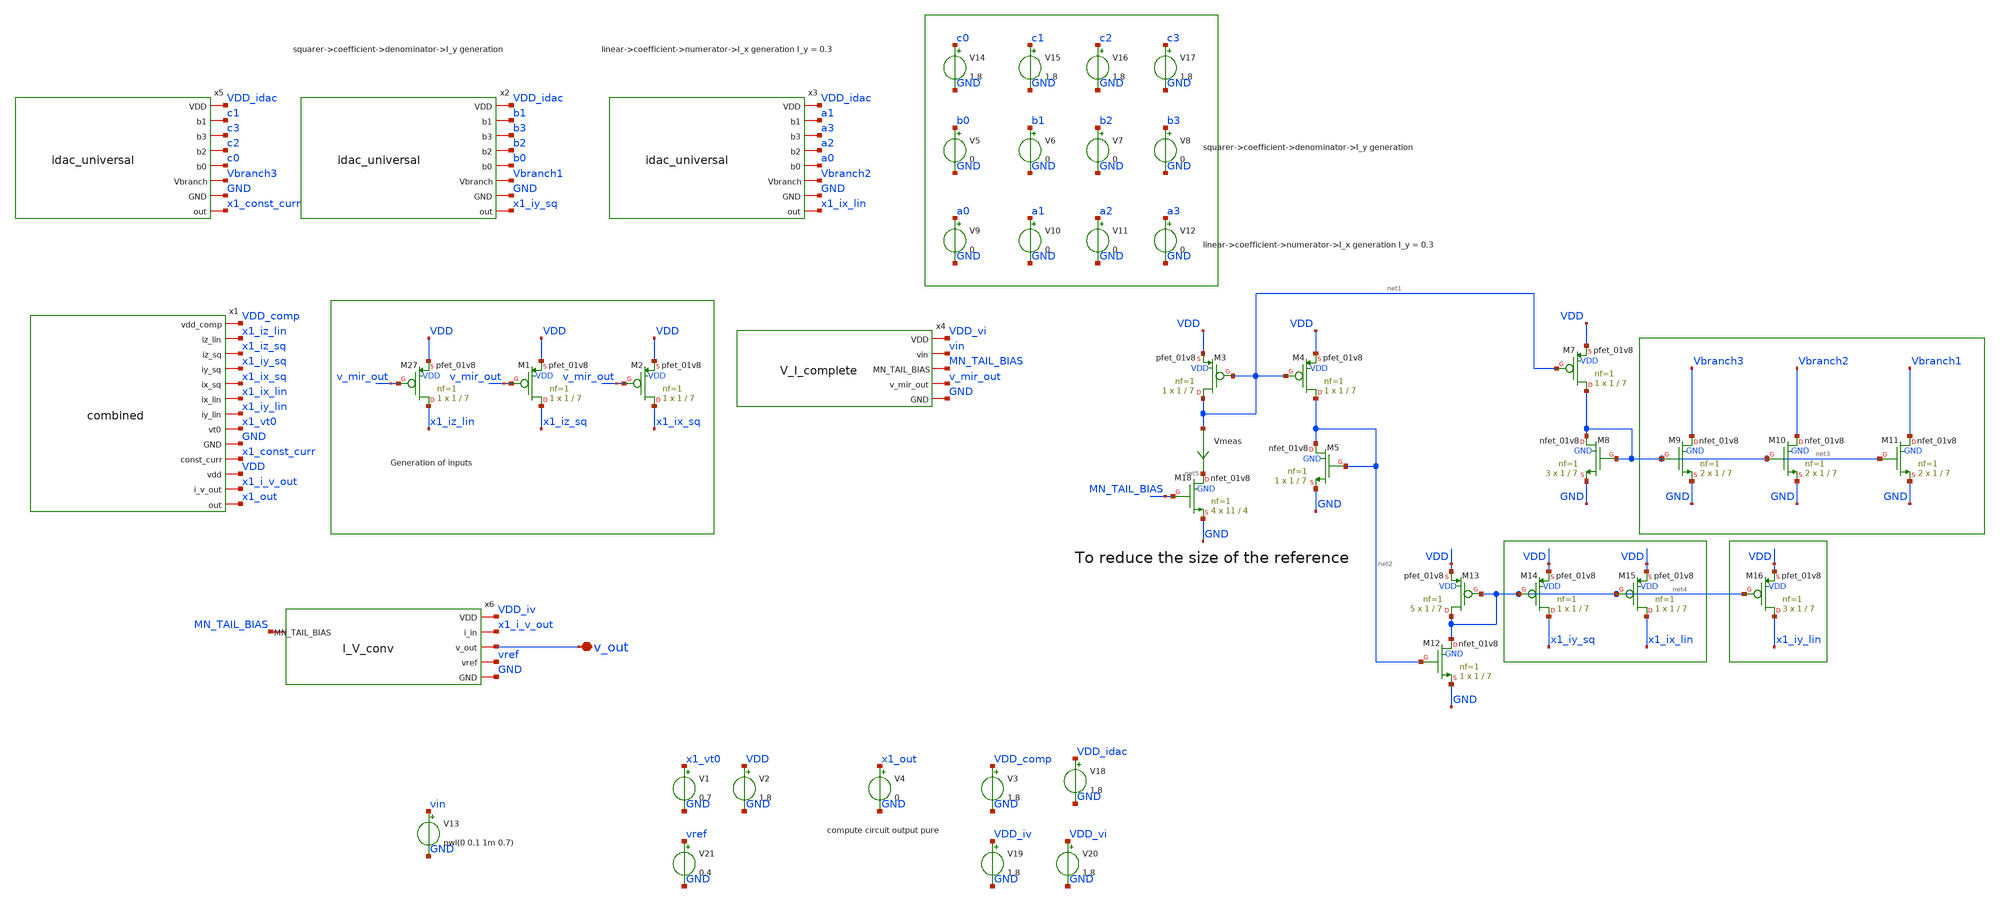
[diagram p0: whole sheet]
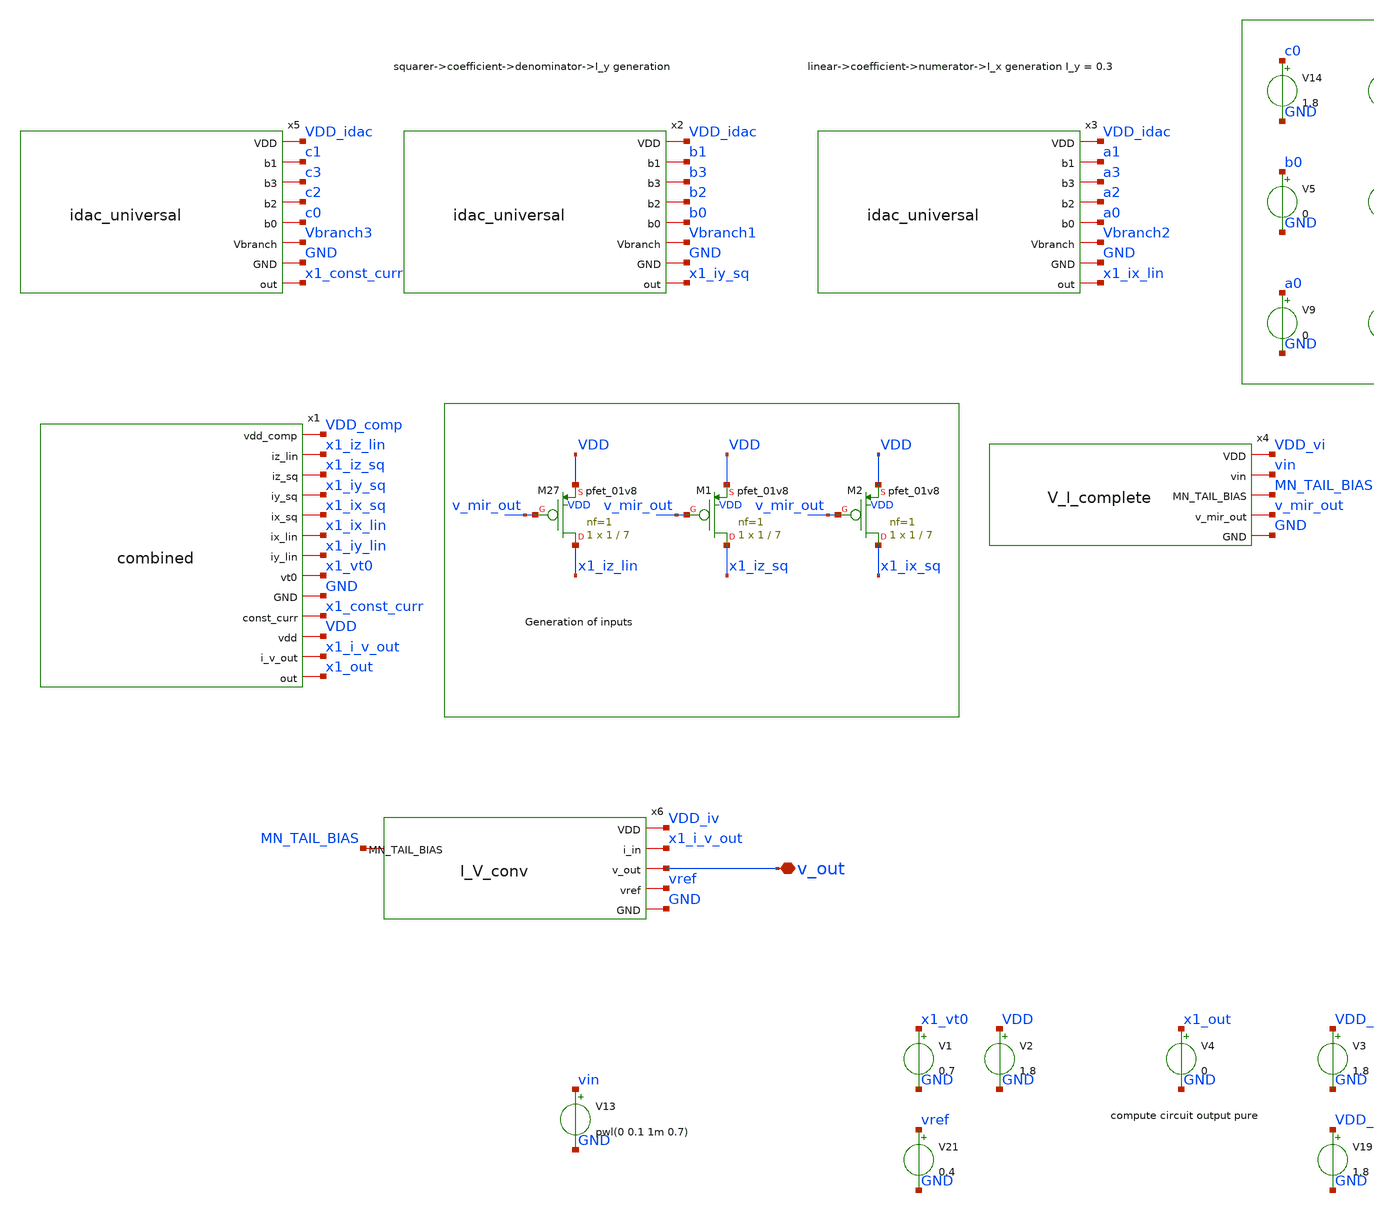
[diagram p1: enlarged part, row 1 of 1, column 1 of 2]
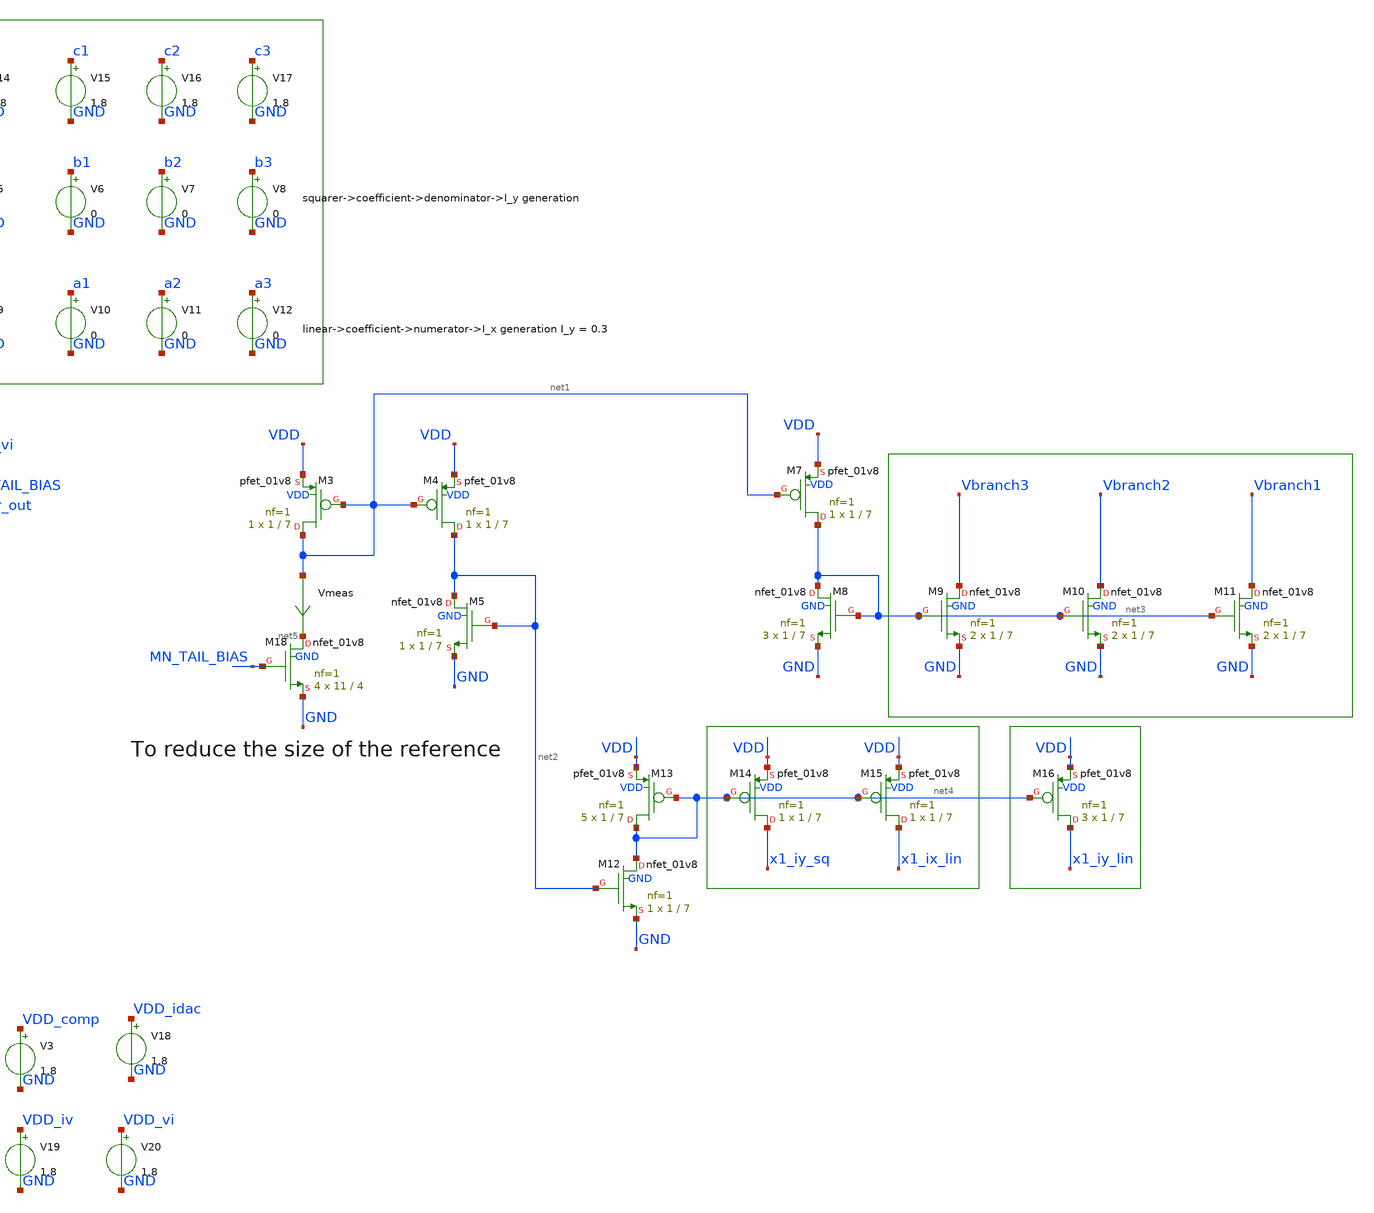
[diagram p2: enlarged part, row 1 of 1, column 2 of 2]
** sch_path: xschem/top/compute_system.sch
**.subckt compute_system v_out
*.iopin v_out
V5 b0 GND 0
V6 b1 GND 0
V7 b2 GND 0
V8 b3 GND 0
V9 a0 GND 0
V10 a1 GND 0
V11 a2 GND 0
V12 a3 GND 0
V1 x1_vt0 GND 0.7
V2 VDD GND 1.8
V4 x1_out GND 0
XM27 x1_iz_lin v_mir_out VDD VDD sky130_fd_pr__pfet_01v8 L=7 W=1 nf=1 ad='int((1 + 1)/2) * 1 / 1 * 0.29'
+ as='int((1 + 2)/2) * 1 / 1 * 0.29' pd='2*int((1 + 1)/2) * (1 / 1 + 0.29)' ps='2*int((1 + 2)/2) * (1 / 1 + 0.29)'
+ nrd='0.29 / 1 ' nrs='0.29 / 1 ' sa=0 sb=0 sd=0 mult=1 m=1
XM1 x1_iz_sq v_mir_out VDD VDD sky130_fd_pr__pfet_01v8 L=7 W=1 nf=1 ad='int((1 + 1)/2) * 1 / 1 * 0.29'
+ as='int((1 + 2)/2) * 1 / 1 * 0.29' pd='2*int((1 + 1)/2) * (1 / 1 + 0.29)' ps='2*int((1 + 2)/2) * (1 / 1 + 0.29)'
+ nrd='0.29 / 1 ' nrs='0.29 / 1 ' sa=0 sb=0 sd=0 mult=1 m=1
XM2 x1_ix_sq v_mir_out VDD VDD sky130_fd_pr__pfet_01v8 L=7 W=1 nf=1 ad='int((1 + 1)/2) * 1 / 1 * 0.29'
+ as='int((1 + 2)/2) * 1 / 1 * 0.29' pd='2*int((1 + 1)/2) * (1 / 1 + 0.29)' ps='2*int((1 + 2)/2) * (1 / 1 + 0.29)'
+ nrd='0.29 / 1 ' nrs='0.29 / 1 ' sa=0 sb=0 sd=0 mult=1 m=1
V14 c0 GND 1.8
V15 c1 GND 1.8
V16 c2 GND 1.8
V17 c3 GND 1.8
XM18 net5 MN_TAIL_BIAS GND GND sky130_fd_pr__nfet_01v8 L=4 W=11 nf=1 ad='int((nf+1)/2) * W/nf * 0.29'
+ as='int((nf+2)/2) * W/nf * 0.29' pd='2*int((nf+1)/2) * (W/nf + 0.29)' ps='2*int((nf+2)/2) * (W/nf + 0.29)'
+ nrd='0.29 / W' nrs='0.29 / W' sa=0 sb=0 sd=0 mult=4 m=4
XM3 net1 net1 VDD VDD sky130_fd_pr__pfet_01v8 L=7 W=1 nf=1 ad='int((1 + 1)/2) * 1 / 1 * 0.29' as='int((1 + 2)/2) * 1 / 1 * 0.29'
+ pd='2*int((1 + 1)/2) * (1 / 1 + 0.29)' ps='2*int((1 + 2)/2) * (1 / 1 + 0.29)' nrd='0.29 / 1 ' nrs='0.29 / 1 '
+ sa=0 sb=0 sd=0 mult=1 m=1
XM4 net2 net1 VDD VDD sky130_fd_pr__pfet_01v8 L=7 W=1 nf=1 ad='int((1 + 1)/2) * 1 / 1 * 0.29' as='int((1 + 2)/2) * 1 / 1 * 0.29'
+ pd='2*int((1 + 1)/2) * (1 / 1 + 0.29)' ps='2*int((1 + 2)/2) * (1 / 1 + 0.29)' nrd='0.29 / 1 ' nrs='0.29 / 1 '
+ sa=0 sb=0 sd=0 mult=1 m=1
XM5 net2 net2 GND GND sky130_fd_pr__nfet_01v8 L=7 W=1 nf=1 ad='int((nf+1)/2) * W/nf * 0.29' as='int((nf+2)/2) * W/nf * 0.29'
+ pd='2*int((nf+1)/2) * (W/nf + 0.29)' ps='2*int((nf+2)/2) * (W/nf + 0.29)' nrd='0.29 / W' nrs='0.29 / W'
+ sa=0 sb=0 sd=0 mult=1 m=1
Vmeas net1 net5 0
.save i(vmeas)
XM7 net3 net1 VDD VDD sky130_fd_pr__pfet_01v8 L=7 W=1 nf=1 ad='int((1 + 1)/2) * 1 / 1 * 0.29' as='int((1 + 2)/2) * 1 / 1 * 0.29'
+ pd='2*int((1 + 1)/2) * (1 / 1 + 0.29)' ps='2*int((1 + 2)/2) * (1 / 1 + 0.29)' nrd='0.29 / 1 ' nrs='0.29 / 1 '
+ sa=0 sb=0 sd=0 mult=1 m=1
XM8 net3 net3 GND GND sky130_fd_pr__nfet_01v8 L=7 W=1 nf=1 ad='int((nf+1)/2) * W/nf * 0.29' as='int((nf+2)/2) * W/nf * 0.29'
+ pd='2*int((nf+1)/2) * (W/nf + 0.29)' ps='2*int((nf+2)/2) * (W/nf + 0.29)' nrd='0.29 / W' nrs='0.29 / W'
+ sa=0 sb=0 sd=0 mult=3 m=3
XM9 Vbranch3 net3 GND GND sky130_fd_pr__nfet_01v8 L=7 W=1 nf=1 ad='int((nf+1)/2) * W/nf * 0.29' as='int((nf+2)/2) * W/nf * 0.29'
+ pd='2*int((nf+1)/2) * (W/nf + 0.29)' ps='2*int((nf+2)/2) * (W/nf + 0.29)' nrd='0.29 / W' nrs='0.29 / W'
+ sa=0 sb=0 sd=0 mult=2 m=2
XM10 Vbranch2 net3 GND GND sky130_fd_pr__nfet_01v8 L=7 W=1 nf=1 ad='int((nf+1)/2) * W/nf * 0.29' as='int((nf+2)/2) * W/nf * 0.29'
+ pd='2*int((nf+1)/2) * (W/nf + 0.29)' ps='2*int((nf+2)/2) * (W/nf + 0.29)' nrd='0.29 / W' nrs='0.29 / W'
+ sa=0 sb=0 sd=0 mult=2 m=2
XM11 Vbranch1 net3 GND GND sky130_fd_pr__nfet_01v8 L=7 W=1 nf=1 ad='int((nf+1)/2) * W/nf * 0.29' as='int((nf+2)/2) * W/nf * 0.29'
+ pd='2*int((nf+1)/2) * (W/nf + 0.29)' ps='2*int((nf+2)/2) * (W/nf + 0.29)' nrd='0.29 / W' nrs='0.29 / W'
+ sa=0 sb=0 sd=0 mult=2 m=2
XM12 net4 net2 GND GND sky130_fd_pr__nfet_01v8 L=7 W=1 nf=1 ad='int((nf+1)/2) * W/nf * 0.29' as='int((nf+2)/2) * W/nf * 0.29'
+ pd='2*int((nf+1)/2) * (W/nf + 0.29)' ps='2*int((nf+2)/2) * (W/nf + 0.29)' nrd='0.29 / W' nrs='0.29 / W'
+ sa=0 sb=0 sd=0 mult=1 m=1
XM13 net4 net4 VDD VDD sky130_fd_pr__pfet_01v8 L=7 W=1 nf=1 ad='int((1 + 1)/2) * 1 / 1 * 0.29' as='int((1 + 2)/2) * 1 / 1 * 0.29'
+ pd='2*int((1 + 1)/2) * (1 / 1 + 0.29)' ps='2*int((1 + 2)/2) * (1 / 1 + 0.29)' nrd='0.29 / 1 ' nrs='0.29 / 1 '
+ sa=0 sb=0 sd=0 mult=5 m=5
XM14 x1_iy_sq net4 VDD VDD sky130_fd_pr__pfet_01v8 L=7 W=1 nf=1 ad='int((1 + 1)/2) * 1 / 1 * 0.29' as='int((1 + 2)/2) * 1 / 1 * 0.29'
+ pd='2*int((1 + 1)/2) * (1 / 1 + 0.29)' ps='2*int((1 + 2)/2) * (1 / 1 + 0.29)' nrd='0.29 / 1 ' nrs='0.29 / 1 '
+ sa=0 sb=0 sd=0 mult=1 m=1
XM15 x1_ix_lin net4 VDD VDD sky130_fd_pr__pfet_01v8 L=7 W=1 nf=1 ad='int((1 + 1)/2) * 1 / 1 * 0.29' as='int((1 + 2)/2) * 1 / 1 * 0.29'
+ pd='2*int((1 + 1)/2) * (1 / 1 + 0.29)' ps='2*int((1 + 2)/2) * (1 / 1 + 0.29)' nrd='0.29 / 1 ' nrs='0.29 / 1 '
+ sa=0 sb=0 sd=0 mult=1 m=1
XM16 x1_iy_lin net4 VDD VDD sky130_fd_pr__pfet_01v8 L=7 W=1 nf=1 ad='int((1 + 1)/2) * 1 / 1 * 0.29' as='int((1 + 2)/2) * 1 / 1 * 0.29'
+ pd='2*int((1 + 1)/2) * (1 / 1 + 0.29)' ps='2*int((1 + 2)/2) * (1 / 1 + 0.29)' nrd='0.29 / 1 ' nrs='0.29 / 1 '
+ sa=0 sb=0 sd=0 mult=3 m=3
x5 VDD_idac c1 c3 c2 c0 Vbranch3 GND x1_const_curr idac_universal
x2 VDD_idac b1 b3 b2 b0 Vbranch1 GND x1_iy_sq idac_universal
x3 VDD_idac a1 a3 a2 a0 Vbranch2 GND x1_ix_lin idac_universal
x1 VDD_comp x1_iz_lin x1_iz_sq x1_iy_sq x1_ix_sq x1_ix_lin x1_iy_lin x1_vt0 GND x1_const_curr VDD
+ x1_i_v_out x1_out combined
x6 VDD_iv x1_i_v_out v_out vref GND MN_TAIL_BIAS I_V_conv
x4 VDD_vi vin MN_TAIL_BIAS v_mir_out GND V_I_complete
V3 VDD_comp GND 1.8
V18 VDD_idac GND 1.8
V19 VDD_iv GND 1.8
V20 VDD_vi GND 1.8
V21 vref GND 0.4
V13 vin GND pwl(0 0.1 1m 0.7)
**** begin user architecture code


.options savecurrents
.options rshunt=1e12 method=gear
*.options reltol=1e-3 abstol=1e-12
.control

save all
* dc V13 0 0.7 0.005
tran 1u 1m
set filetype=ascii
write IDAC_poly_V_I.raw
plot v(v_out)
plot @m.xm1.msky130_fd_pr__pfet_01v8[id]
plot i(v4)
.endc



** opencircuitdesign pdks install
.lib $::SKYWATER_MODELS/sky130.lib.spice tt

**** end user architecture code
**.ends
.end
